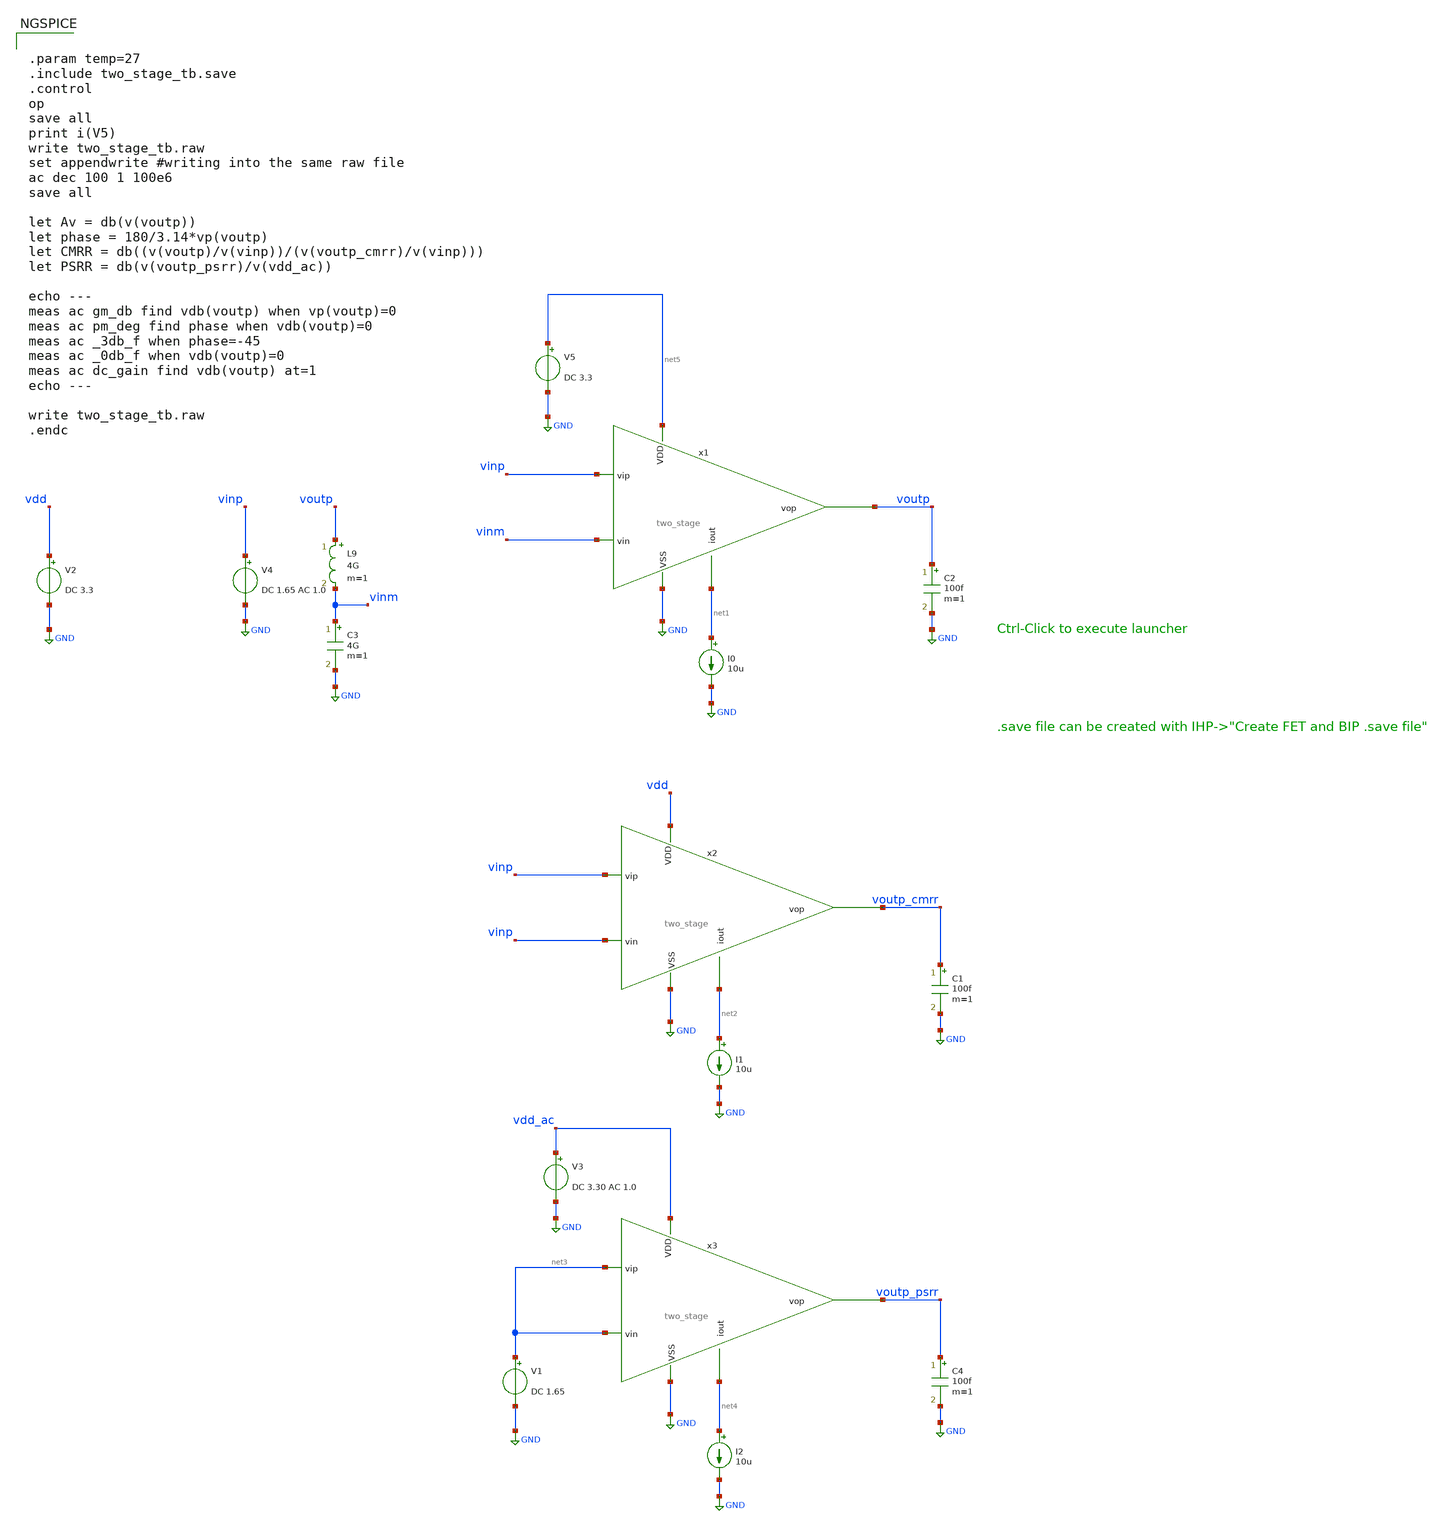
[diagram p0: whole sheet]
** sch_path: testbench/two_stage_tb.sch
**.subckt two_stage_tb
C2 voutp GND 100f m=1
V2 vdd GND DC 3.3
V4 vinp GND DC 1.65 AC 1.0
L9 voutp vinm 4G m=1
C3 vinm GND 4G m=1
x1 net5 voutp vinp vinm GND net1 two_stage
I0 net1 GND 10u
C1 voutp_cmrr GND 100f m=1
x2 vdd voutp_cmrr vinp vinp GND net2 two_stage
I1 net2 GND 10u
C4 voutp_psrr GND 100f m=1
x3 vdd_ac voutp_psrr net3 net3 GND net4 two_stage
I2 net4 GND 10u
V1 net3 GND DC 1.65
V3 vdd_ac GND DC 3.30 AC 1.0
V5 net5 GND DC 3.3
**** begin user architecture code

.lib cornerMOShv.lib mos_tt
.lib $::SG13G2_MODELS/cornerCAP.lib cap_typ



.param temp=27
.include two_stage_tb.save
.control
op
save all
print i(V5)
write two_stage_tb.raw
set appendwrite #writing into the same raw file
ac dec 100 1 100e6
save all

let Av = db(v(voutp))
let phase = 180/3.14*vp(voutp)
let CMRR = db((v(voutp)/v(vinp))/(v(voutp_cmrr)/v(vinp)))
let PSRR = db(v(voutp_psrr)/v(vdd_ac))

echo ---
meas ac gm_db find vdb(voutp) when vp(voutp)=0
meas ac pm_deg find phase when vdb(voutp)=0
meas ac _3db_f when phase=-45
meas ac _0db_f when vdb(voutp)=0
meas ac dc_gain find vdb(voutp) at=1
echo ---

write two_stage_tb.raw
.endc


**** end user architecture code
**.ends

* expanding   symbol:  two_stage.sym # of pins=6
** sym_path: schematic/two_stage.sym
** sch_path: schematic/two_stage.sch
.subckt two_stage vdd out v+ v- vss iout
*.opin out
*.ipin iout
*.ipin v-
*.ipin v+
*.ipin vdd
*.ipin vss
XM1 net2 v- net1 vdd sg13_hv_pmos w=23.0u l=5.0u ng=5 m=1 mm_ok=1
XM2 net3 v+ net1 vdd sg13_hv_pmos w=23.0u l=5.0u ng=5 m=1 mm_ok=1
XM5 mirror vb_n net5 vss sg13_hv_nmos w=0.370u l=2.0u ng=1 m=1 mm_ok=1
XM11 net1 iout vdd vdd sg13_hv_pmos w=1.0u l=5.0u ng=1 m=1 mm_ok=1
XM12 iout iout vdd vdd sg13_hv_pmos w=8.5u l=5.0u ng=1 m=1 mm_ok=1
XM3 mirror vb_p net2 vdd sg13_hv_pmos w=1.3u l=1.0u ng=1 m=1 mm_ok=1
XM4 net4 vb_p net3 vdd sg13_hv_pmos w=1.3u l=1.0u ng=1 m=1 mm_ok=1
XM6 net4 vb_n net6 vss sg13_hv_nmos w=0.370u l=2.0u ng=1 m=1 mm_ok=1
XM7 net5 mirror vss vss sg13_hv_nmos w=0.370u l=2.0u ng=1 m=1 mm_ok=1
XM8 net6 mirror vss vss sg13_hv_nmos w=0.370u l=2.0u ng=1 m=1 mm_ok=1
XM9 out net4 vss vss sg13_hv_nmos w=2.35u l=5.00u ng=1 m=1 mm_ok=1
XC1 net4 out cap_cmim w=10.0e-6 l=10.0e-6 m=1 mm_ok=1
XM10 out iout vdd vdd sg13_hv_pmos w=8.5u l=5.0u ng=1 m=1 mm_ok=1
V1 vb_p vss 1.0
V2 vb_n vss 2.0
.ends

.GLOBAL GND
.end
